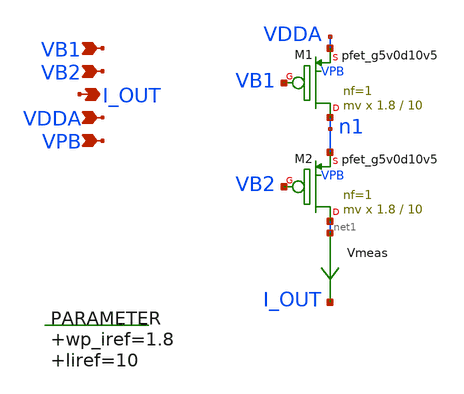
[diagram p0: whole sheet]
** sch_path: xschem/head.sch
**.subckt head I_OUT VB1 VB2 VDDA VPB
*.opin I_OUT
*.ipin VB1
*.ipin VB2
*.ipin VDDA
*.ipin VPB
XM1 n1 VB1 VDDA VPB sky130_fd_pr__pfet_g5v0d10v5 L=10 W=1.8 nf=1 ad='int((nf+1)/2) * W/nf * 0.29' as='int((nf+2)/2) * W/nf * 0.29'
+ pd='2*int((nf+1)/2) * (W/nf + 0.29)' ps='2*int((nf+2)/2) * (W/nf + 0.29)' nrd='0.29 / W' nrs='0.29 / W'
+ sa=0 sb=0 sd=0 mult=mv m=mv
.param wp_iref=1.8 liref=10

Vmeas net1 I_OUT 0
.save i(vmeas)
XM2 net1 VB2 n1 VPB sky130_fd_pr__pfet_g5v0d10v5 L=10 W=1.8 nf=1 ad='int((nf+1)/2) * W/nf * 0.29' as='int((nf+2)/2) * W/nf * 0.29'
+ pd='2*int((nf+1)/2) * (W/nf + 0.29)' ps='2*int((nf+2)/2) * (W/nf + 0.29)' nrd='0.29 / W' nrs='0.29 / W'
+ sa=0 sb=0 sd=0 mult=mv m=mv
**.ends
.end
